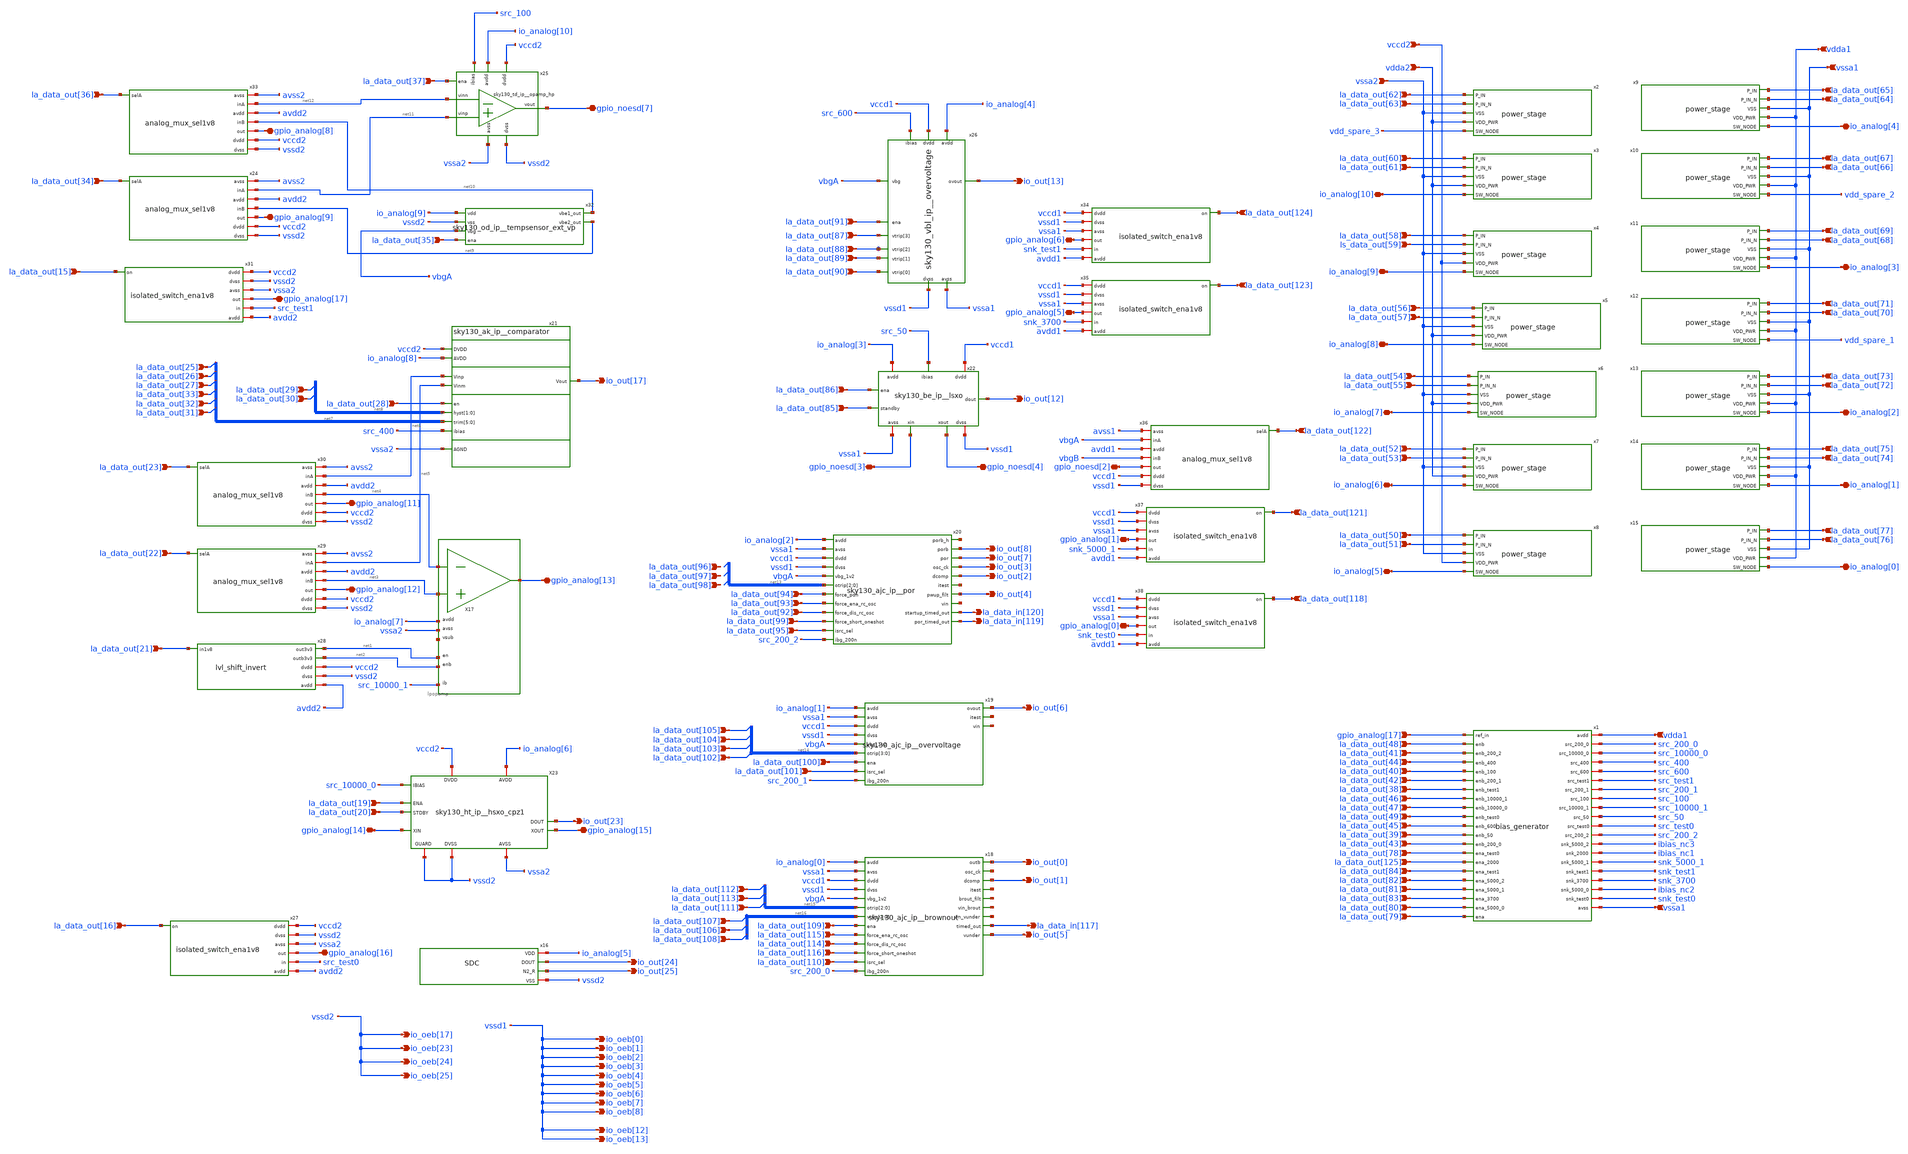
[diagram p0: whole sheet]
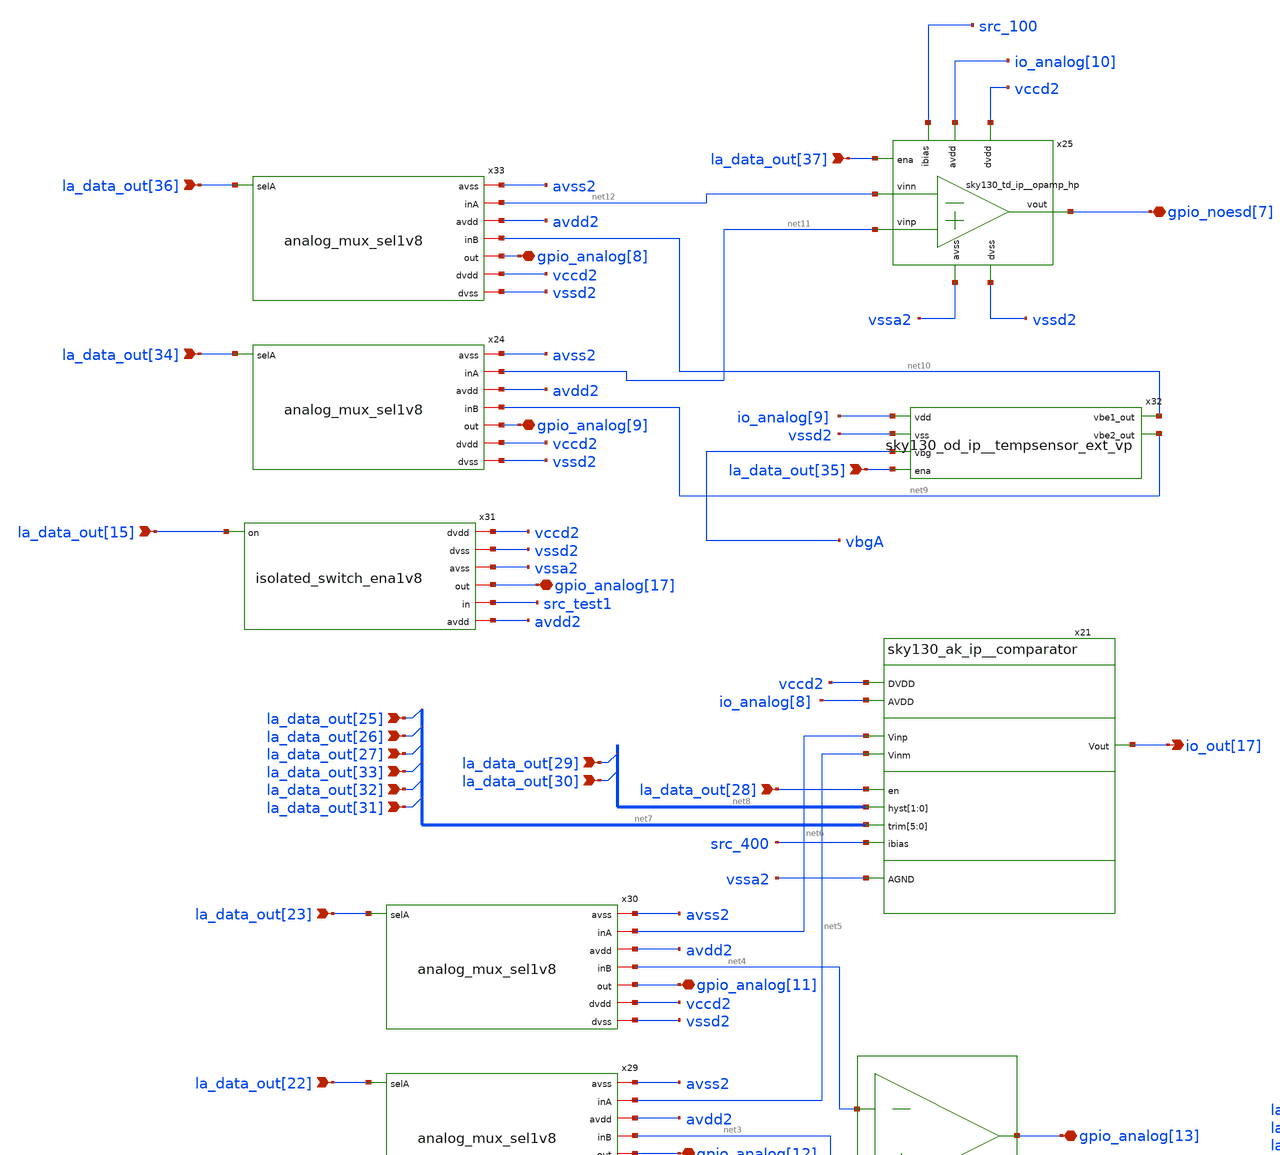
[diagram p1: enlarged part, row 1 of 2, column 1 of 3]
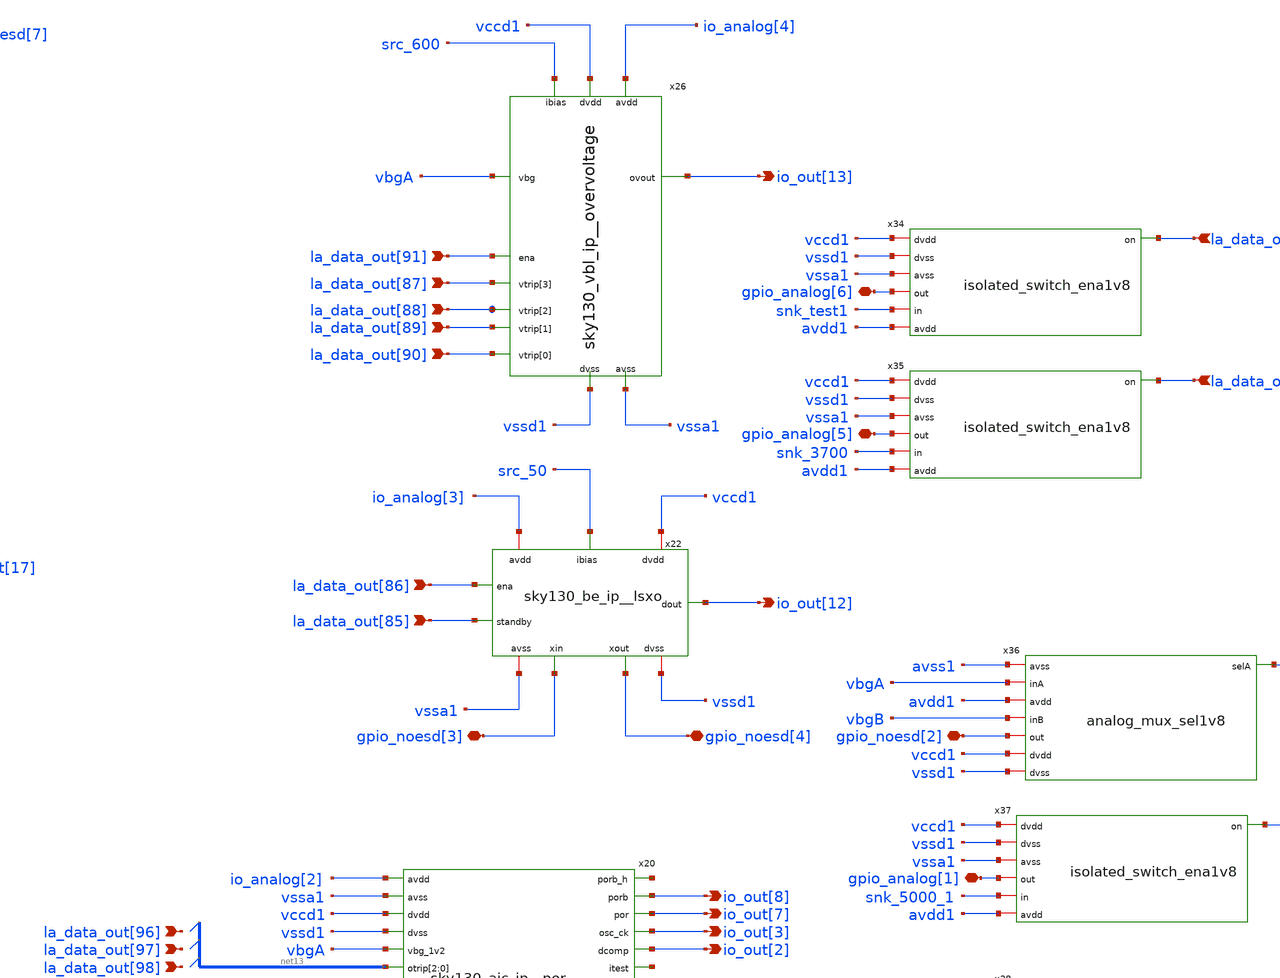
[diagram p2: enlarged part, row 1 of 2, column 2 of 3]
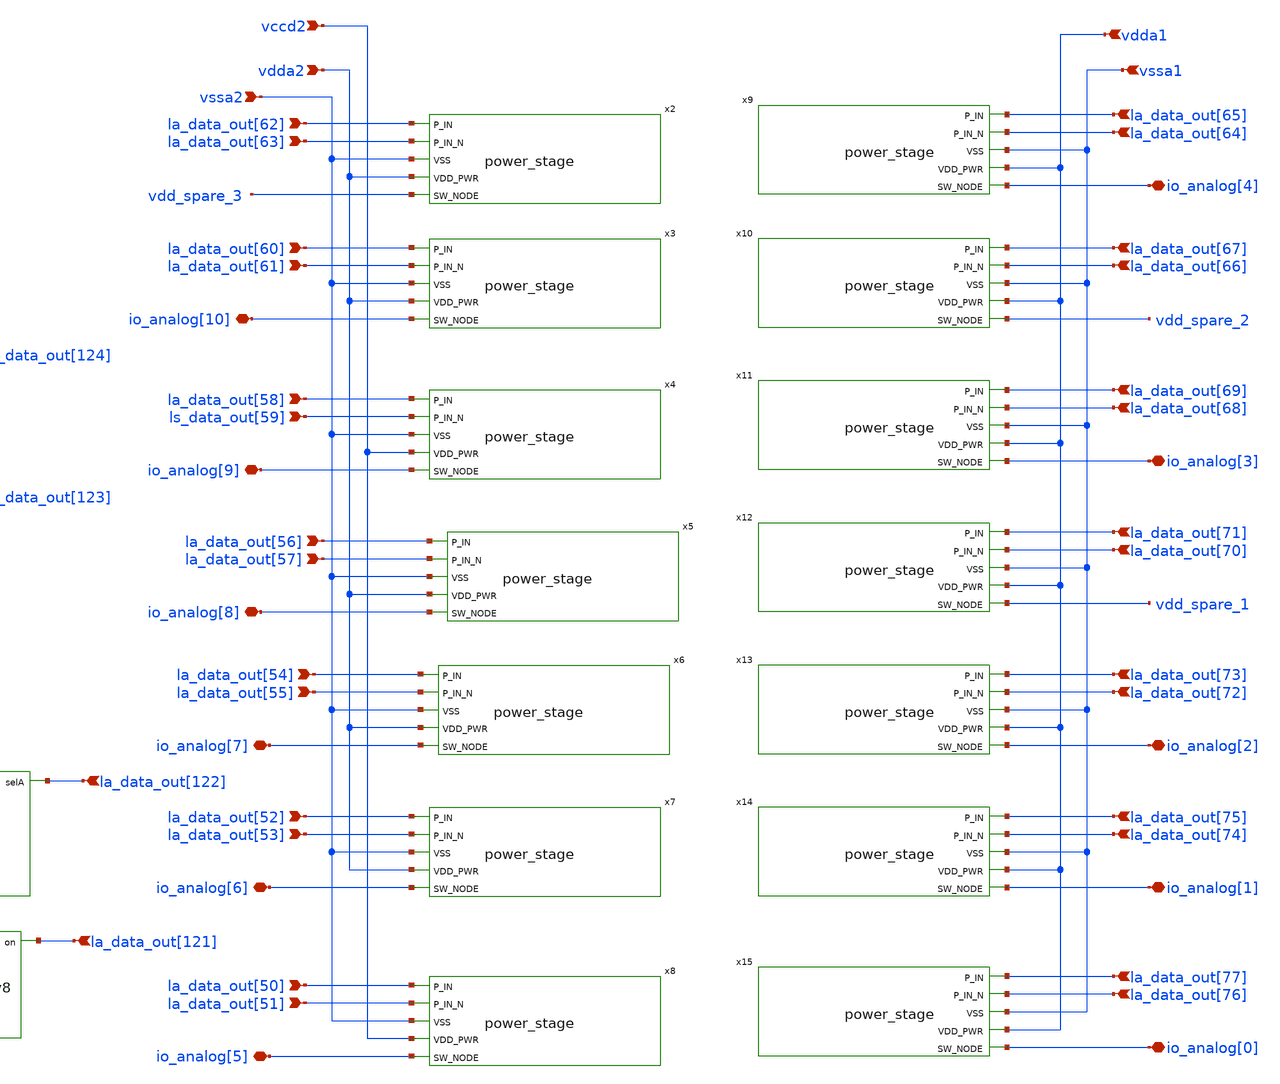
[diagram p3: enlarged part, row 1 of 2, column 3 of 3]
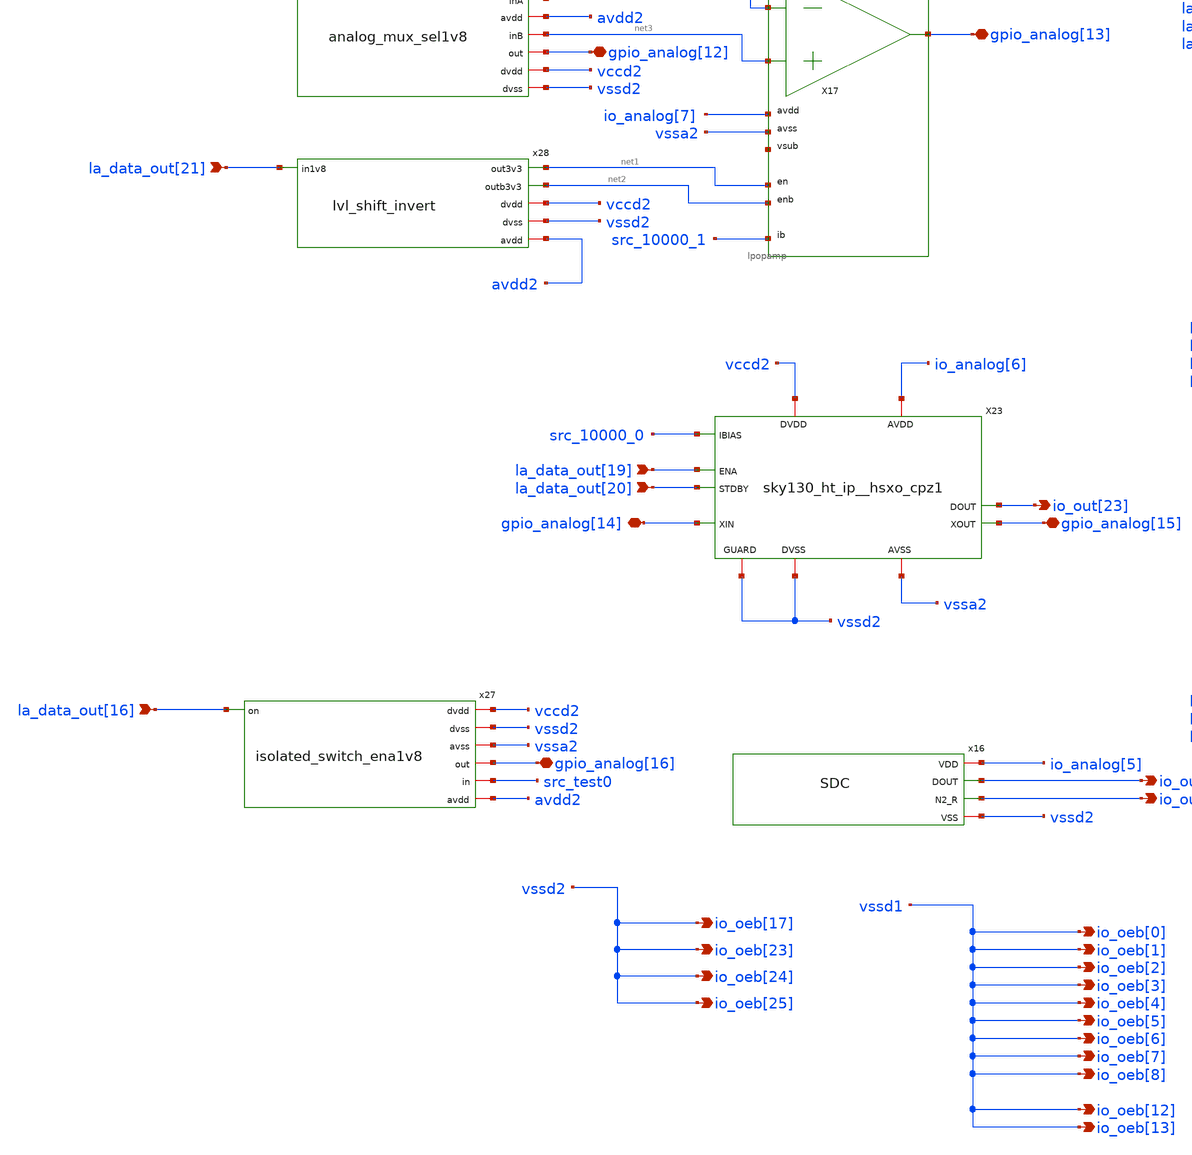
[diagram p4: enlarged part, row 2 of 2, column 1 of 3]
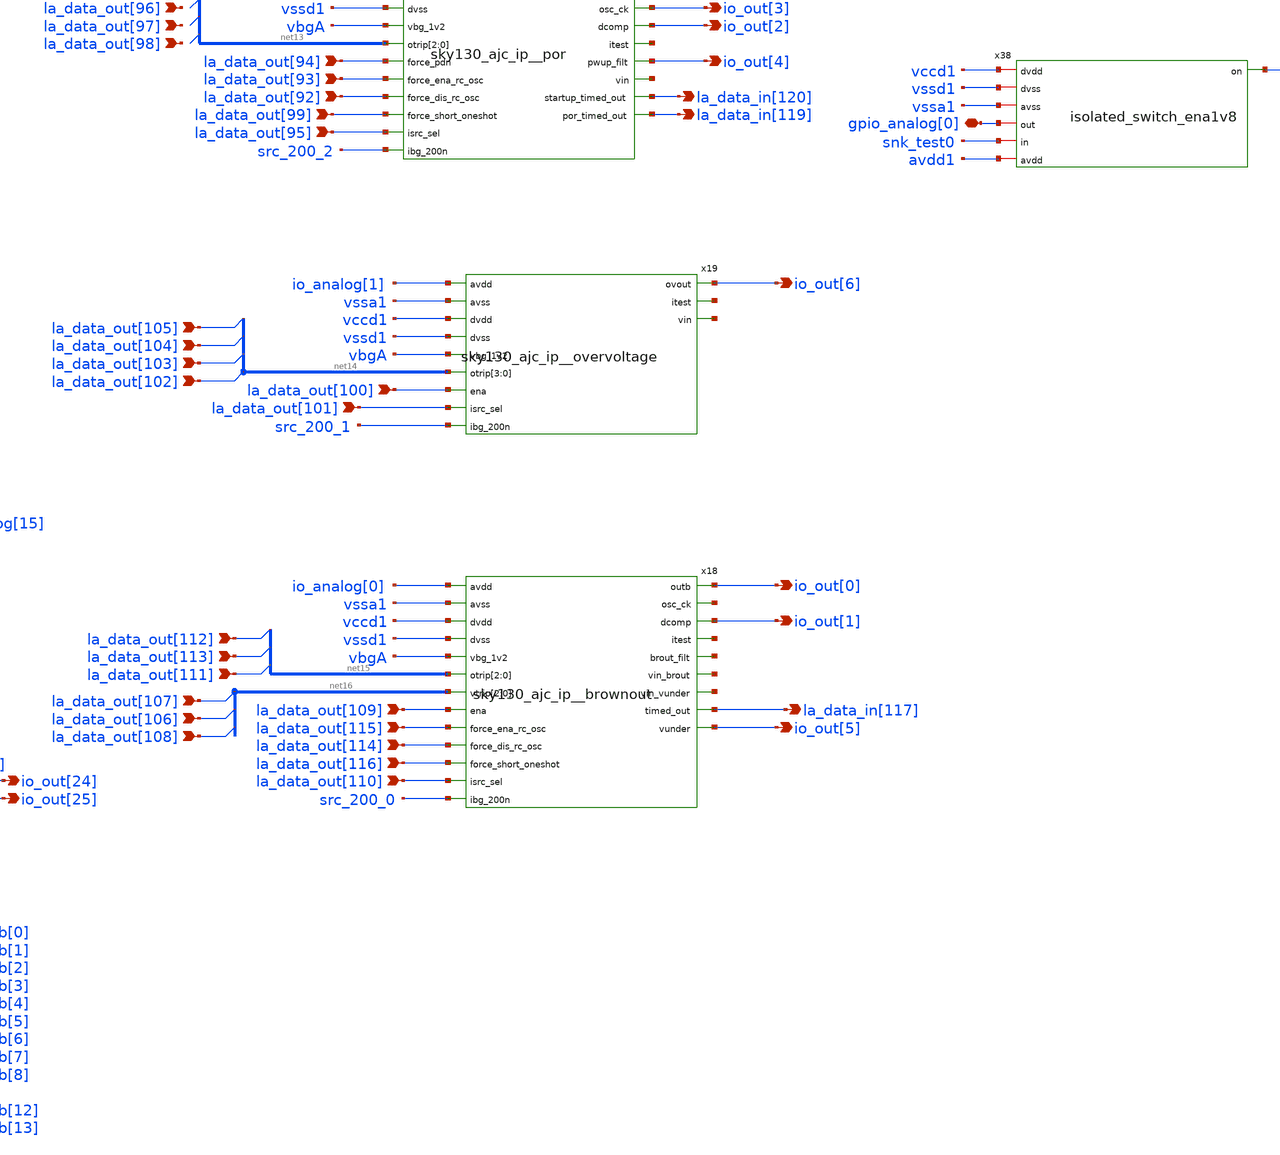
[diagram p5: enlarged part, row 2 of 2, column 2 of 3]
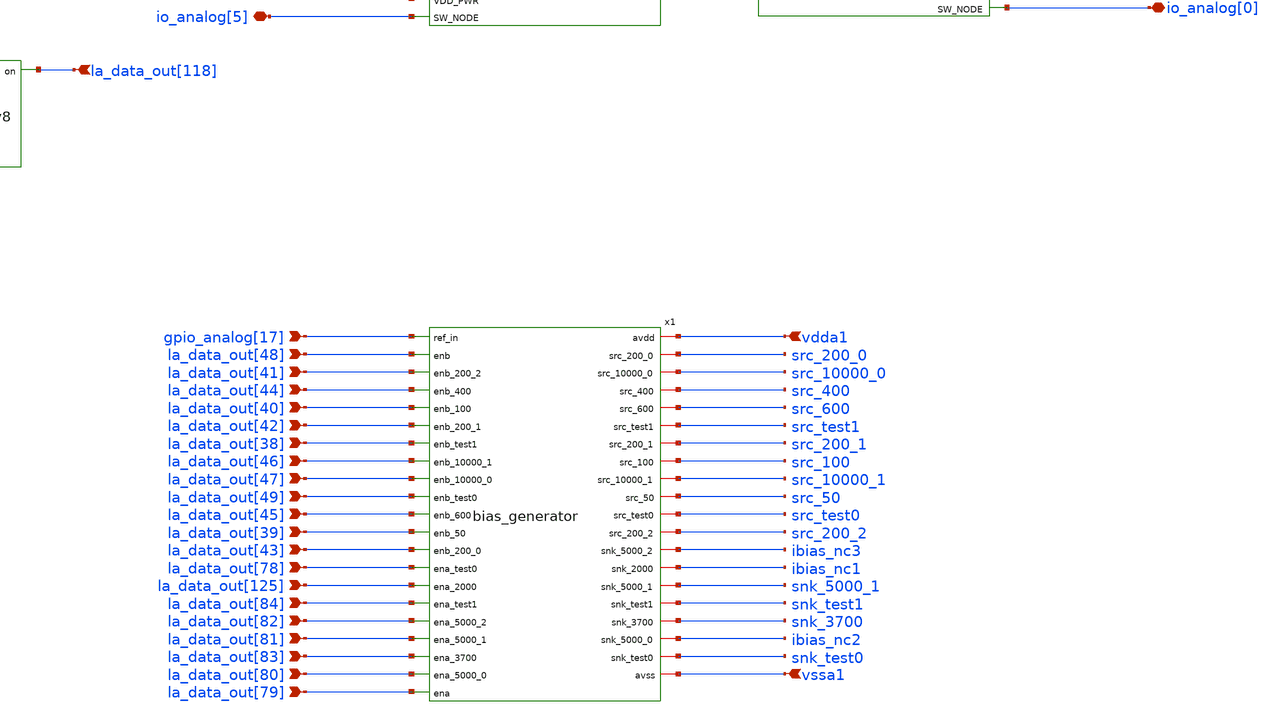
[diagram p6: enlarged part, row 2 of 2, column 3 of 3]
** sch_path: xschem/chipalooza_testchip1.sch
**.subckt chipalooza_testchip1 vdda1 vssa1 vccd2 vdda2 vssa2 la_data_out[50] la_data_out[51]
*+ la_data_out[62] la_data_out[63] la_data_out[60] la_data_out[61] la_data_out[58] ls_data_out[59] la_data_out[56]
*+ la_data_out[57] la_data_out[54] la_data_out[55] la_data_out[52] la_data_out[53] la_data_out[77] la_data_out[76]
*+ la_data_out[75] la_data_out[74] la_data_out[73] la_data_out[72] la_data_out[71] la_data_out[70] la_data_out[69]
*+ la_data_out[68] la_data_out[67] la_data_out[66] la_data_out[65] la_data_out[64] gpio_analog[17] la_data_out[49]
*+ la_data_out[48] la_data_out[47] la_data_out[46] la_data_out[45] la_data_out[44] la_data_out[43] la_data_out[42]
*+ la_data_out[41] la_data_out[40] la_data_out[39] la_data_out[38] la_data_out[84] la_data_out[83] la_data_out[82]
*+ la_data_out[81] la_data_out[80] la_data_out[79] la_data_out[78] la_data_out[125] vssa1 vdda1 io_out[25] io_out[24]
*+ gpio_analog[16] gpio_analog[14] gpio_analog[15] la_data_out[19] la_data_out[20] io_out[23] la_data_out[16]
*+ gpio_analog[13] la_data_out[21] gpio_analog[12] gpio_analog[11] la_data_out[22] la_data_out[23] la_data_out[33]
*+ la_data_out[32] la_data_out[31] la_data_out[27] la_data_out[26] la_data_out[25] io_out[17] la_data_out[30]
*+ la_data_out[29] la_data_out[28] gpio_analog[17] la_data_out[15] la_data_out[34] la_data_out[36] gpio_analog[9]
*+ gpio_analog[8] la_data_out[35] la_data_out[37] gpio_noesd[7] io_out[13] la_data_out[91] la_data_out[90]
*+ la_data_out[89] la_data_out[88] la_data_out[87] gpio_analog[6] la_data_out[124] gpio_analog[5] la_data_out[123]
*+ io_out[12] gpio_noesd[4] gpio_noesd[3] la_data_out[85] la_data_out[86] gpio_noesd[2] la_data_out[122]
*+ gpio_analog[1] la_data_out[121] gpio_analog[0] la_data_out[118] io_out[2] io_out[7] io_out[8] io_out[3]
*+ la_data_in[119] la_data_out[92] la_data_out[93] la_data_out[94] io_out[4] la_data_out[98] la_data_out[97]
*+ la_data_out[96] la_data_out[95] la_data_out[99] la_data_in[120] io_out[6] la_data_out[105] la_data_out[104]
*+ la_data_out[103] la_data_out[102] la_data_out[101] la_data_out[100] io_out[0] io_out[5] la_data_out[107]
*+ la_data_out[106] la_data_out[108] la_data_in[117] la_data_out[116] io_out[1] la_data_out[115] la_data_out[114]
*+ la_data_out[112] la_data_out[113] la_data_out[111] la_data_out[110] la_data_out[109] io_oeb[0] io_oeb[1] io_oeb[2]
*+ io_oeb[3] io_oeb[4] io_oeb[5] io_oeb[6] io_oeb[7] io_oeb[8] io_oeb[12] io_oeb[13] io_oeb[17] io_oeb[23]
*+ io_oeb[24] io_oeb[25] io_analog[10] io_analog[9] io_analog[8] io_analog[7] io_analog[6] io_analog[5]
*+ io_analog[0] io_analog[1] io_analog[2] io_analog[3] io_analog[4]
*.ipin vdda1
*.ipin vssa1
*.ipin vccd2
*.ipin vdda2
*.ipin vssa2
*.ipin la_data_out[50]
*.ipin la_data_out[51]
*.ipin la_data_out[62]
*.ipin la_data_out[63]
*.ipin la_data_out[60]
*.ipin la_data_out[61]
*.ipin la_data_out[58]
*.ipin ls_data_out[59]
*.ipin la_data_out[56]
*.ipin la_data_out[57]
*.ipin la_data_out[54]
*.ipin la_data_out[55]
*.ipin la_data_out[52]
*.ipin la_data_out[53]
*.ipin la_data_out[77]
*.ipin la_data_out[76]
*.ipin la_data_out[75]
*.ipin la_data_out[74]
*.ipin la_data_out[73]
*.ipin la_data_out[72]
*.ipin la_data_out[71]
*.ipin la_data_out[70]
*.ipin la_data_out[69]
*.ipin la_data_out[68]
*.ipin la_data_out[67]
*.ipin la_data_out[66]
*.ipin la_data_out[65]
*.ipin la_data_out[64]
*.ipin gpio_analog[17]
*.ipin la_data_out[49]
*.ipin la_data_out[48]
*.ipin la_data_out[47]
*.ipin la_data_out[46]
*.ipin la_data_out[45]
*.ipin la_data_out[44]
*.ipin la_data_out[43]
*.ipin la_data_out[42]
*.ipin la_data_out[41]
*.ipin la_data_out[40]
*.ipin la_data_out[39]
*.ipin la_data_out[38]
*.ipin la_data_out[84]
*.ipin la_data_out[83]
*.ipin la_data_out[82]
*.ipin la_data_out[81]
*.ipin la_data_out[80]
*.ipin la_data_out[79]
*.ipin la_data_out[78]
*.ipin la_data_out[125]
*.ipin vssa1
*.ipin vdda1
*.opin io_out[25]
*.opin io_out[24]
*.iopin gpio_analog[16]
*.iopin gpio_analog[14]
*.iopin gpio_analog[15]
*.ipin la_data_out[19]
*.ipin la_data_out[20]
*.opin io_out[23]
*.ipin la_data_out[16]
*.iopin gpio_analog[13]
*.ipin la_data_out[21]
*.iopin gpio_analog[12]
*.iopin gpio_analog[11]
*.ipin la_data_out[22]
*.ipin la_data_out[23]
*.ipin la_data_out[33]
*.ipin la_data_out[32]
*.ipin la_data_out[31]
*.ipin la_data_out[27]
*.ipin la_data_out[26]
*.ipin la_data_out[25]
*.opin io_out[17]
*.ipin la_data_out[30]
*.ipin la_data_out[29]
*.ipin la_data_out[28]
*.iopin gpio_analog[17]
*.ipin la_data_out[15]
*.ipin la_data_out[34]
*.ipin la_data_out[36]
*.iopin gpio_analog[9]
*.iopin gpio_analog[8]
*.ipin la_data_out[35]
*.ipin la_data_out[37]
*.iopin gpio_noesd[7]
*.opin io_out[13]
*.ipin la_data_out[91]
*.ipin la_data_out[90]
*.ipin la_data_out[89]
*.ipin la_data_out[88]
*.ipin la_data_out[87]
*.iopin gpio_analog[6]
*.ipin la_data_out[124]
*.iopin gpio_analog[5]
*.ipin la_data_out[123]
*.opin io_out[12]
*.iopin gpio_noesd[4]
*.iopin gpio_noesd[3]
*.ipin la_data_out[85]
*.ipin la_data_out[86]
*.iopin gpio_noesd[2]
*.ipin la_data_out[122]
*.iopin gpio_analog[1]
*.ipin la_data_out[121]
*.iopin gpio_analog[0]
*.ipin la_data_out[118]
*.opin io_out[2]
*.opin io_out[7]
*.opin io_out[8]
*.opin io_out[3]
*.opin la_data_in[119]
*.ipin la_data_out[92]
*.ipin la_data_out[93]
*.ipin la_data_out[94]
*.opin io_out[4]
*.ipin la_data_out[98]
*.ipin la_data_out[97]
*.ipin la_data_out[96]
*.ipin la_data_out[95]
*.ipin la_data_out[99]
*.opin la_data_in[120]
*.opin io_out[6]
*.ipin la_data_out[105]
*.ipin la_data_out[104]
*.ipin la_data_out[103]
*.ipin la_data_out[102]
*.ipin la_data_out[101]
*.ipin la_data_out[100]
*.opin io_out[0]
*.opin io_out[5]
*.ipin la_data_out[107]
*.ipin la_data_out[106]
*.ipin la_data_out[108]
*.opin la_data_in[117]
*.ipin la_data_out[116]
*.opin io_out[1]
*.ipin la_data_out[115]
*.ipin la_data_out[114]
*.ipin la_data_out[112]
*.ipin la_data_out[113]
*.ipin la_data_out[111]
*.ipin la_data_out[110]
*.ipin la_data_out[109]
*.opin io_oeb[0]
*.opin io_oeb[1]
*.opin io_oeb[2]
*.opin io_oeb[3]
*.opin io_oeb[4]
*.opin io_oeb[5]
*.opin io_oeb[6]
*.opin io_oeb[7]
*.opin io_oeb[8]
*.opin io_oeb[12]
*.opin io_oeb[13]
*.opin io_oeb[17]
*.opin io_oeb[23]
*.opin io_oeb[24]
*.opin io_oeb[25]
*.iopin io_analog[10]
*.iopin io_analog[9]
*.iopin io_analog[8]
*.iopin io_analog[7]
*.iopin io_analog[6]
*.iopin io_analog[5]
*.iopin io_analog[0]
*.iopin io_analog[1]
*.iopin io_analog[2]
*.iopin io_analog[3]
*.iopin io_analog[4]
x1 vdda1 gpio_analog[17] la_data_out[48] la_data_out[41] la_data_out[44] la_data_out[40]
+ la_data_out[42] la_data_out[38] la_data_out[46] la_data_out[47] la_data_out[49] la_data_out[45] la_data_out[39]
+ la_data_out[43] src_200_0 src_10000_0 src_400 src_600 src_test1 src_200_1 src_100 src_10000_1 src_50 src_test0
+ src_200_2 la_data_out[78] la_data_out[125] la_data_out[84] la_data_out[82] la_data_out[81] la_data_out[83]
+ la_data_out[80] ibias_nc3 ibias_nc1 snk_5000_1 snk_test1 snk_3700 ibias_nc2 snk_test0 la_data_out[79] vssa1
+ bias_generator
x2 la_data_out[62] la_data_out[63] vssa2 vdda2 vdd_spare_3 power_stage
x3 la_data_out[60] la_data_out[61] vssa2 vdda2 io_analog[10] power_stage
x4 la_data_out[58] ls_data_out[59] vssa2 vccd2 io_analog[9] power_stage
x5 la_data_out[56] la_data_out[57] vssa2 vdda2 io_analog[8] power_stage
x6 la_data_out[54] la_data_out[55] vssa2 vdda2 io_analog[7] power_stage
x7 la_data_out[52] la_data_out[53] vssa2 vdda2 io_analog[6] power_stage
x8 la_data_out[50] la_data_out[51] vssa2 vccd2 io_analog[5] power_stage
x9 la_data_out[65] la_data_out[64] vssa1 vdda1 io_analog[4] power_stage
x10 la_data_out[67] la_data_out[66] vssa1 vdda1 vdd_spare_2 power_stage
x11 la_data_out[69] la_data_out[68] vssa1 vdda1 io_analog[3] power_stage
x12 la_data_out[71] la_data_out[70] vssa1 vdda1 vdd_spare_1 power_stage
x13 la_data_out[73] la_data_out[72] vssa1 vdda1 io_analog[2] power_stage
x14 la_data_out[75] la_data_out[74] vssa1 vdda1 io_analog[1] power_stage
x15 la_data_out[77] la_data_out[76] vssa1 vdda1 io_analog[0] power_stage
x16 io_analog[5] io_out[24] vssd2 io_out[25] SDC
X17 net4 gpio_analog[13] src_10000_1 net17 vssa2 io_analog[7] net2 net1 net3 lpopamp
x18 io_analog[0] vssa1 io_out[0] vccd1 net18 vssd1 io_out[1] vbgA net15 net15 net15 net19 net20
+ net16 net16 net16 net21 la_data_out[109] la_data_out[115] net22 la_data_out[114] la_data_in[117]
+ io_out[5] la_data_out[116] la_data_out[110] src_200_0 sky130_ajc_ip__brownout
x19 io_analog[1] vssa1 vccd1 vssd1 vbgA io_out[6] net23 net14 net14 net14 net14 net24
+ la_data_out[100] la_data_out[101] src_200_1 sky130_ajc_ip__overvoltage
x20 io_analog[2] net25 io_out[8] vssa1 vccd1 io_out[7] vssd1 io_out[3] vbgA io_out[2] net13 net13
+ net13 net26 la_data_out[94] io_out[4] net27 la_data_out[93] la_data_out[92] la_data_in[120]
+ la_data_in[119] la_data_out[99] la_data_out[95] src_200_2 sky130_ajc_ip__por
x21 vccd2 io_analog[8] vssa2 net6 io_out[17] net5 la_data_out[28] net8 net8 net7 net7 net7 net7 net7
+ net7 src_400 sky130_ak_ip__comparator
x22 io_analog[3] vssa1 vccd1 vssd1 src_50 la_data_out[86] la_data_out[85] io_out[12] gpio_noesd[3]
+ gpio_noesd[4] sky130_be_ip__lsxo
X23 gpio_analog[15] gpio_analog[14] la_data_out[19] la_data_out[20] io_out[23] io_analog[6] vccd2
+ vssa2 vssd2 src_10000_0 vssd2 sky130_ht_ip__hsxo_cpz1
x25 io_analog[10] gpio_noesd[7] src_100 net12 net11 vssa2 vccd2 vssd2 la_data_out[37]
+ sky130_td_ip__opamp_hp
x26 io_analog[4] vccd1 la_data_out[91] la_data_out[87] src_600 la_data_out[88] io_out[13] vbgA
+ la_data_out[89] la_data_out[90] vssd1 vssa1 sky130_vbl_ip__overvoltage
x27 vccd2 vssd2 vssa2 la_data_out[16] gpio_analog[16] src_test0 avdd2 isolated_switch_ena1v8
x28 la_data_out[21] net1 net2 vccd2 vssd2 avdd2 lvl_shift_invert
x29 avss2 la_data_out[22] net5 avdd2 net3 gpio_analog[12] vccd2 vssd2 analog_mux_sel1v8
x30 avss2 la_data_out[23] net6 avdd2 net4 gpio_analog[11] vccd2 vssd2 analog_mux_sel1v8
x31 vccd2 vssd2 vssa2 la_data_out[15] gpio_analog[17] src_test1 avdd2 isolated_switch_ena1v8
x32 net10 io_analog[9] vssd2 vbgA la_data_out[35] net9 sky130_od_ip__tempsensor_ext_vp
x24 avss2 la_data_out[34] net11 avdd2 net9 gpio_analog[9] vccd2 vssd2 analog_mux_sel1v8
x33 avss2 la_data_out[36] net12 avdd2 net10 gpio_analog[8] vccd2 vssd2 analog_mux_sel1v8
x34 vccd1 vssd1 vssa1 la_data_out[124] gpio_analog[6] snk_test1 avdd1 isolated_switch_ena1v8
x35 vccd1 vssd1 vssa1 la_data_out[123] gpio_analog[5] snk_3700 avdd1 isolated_switch_ena1v8
x36 avss1 la_data_out[122] vbgA avdd1 vbgB gpio_noesd[2] vccd1 vssd1 analog_mux_sel1v8
x37 vccd1 vssd1 vssa1 la_data_out[121] gpio_analog[1] snk_5000_1 avdd1 isolated_switch_ena1v8
x38 vccd1 vssd1 vssa1 la_data_out[118] gpio_analog[0] snk_test0 avdd1 isolated_switch_ena1v8
**.ends
.end
